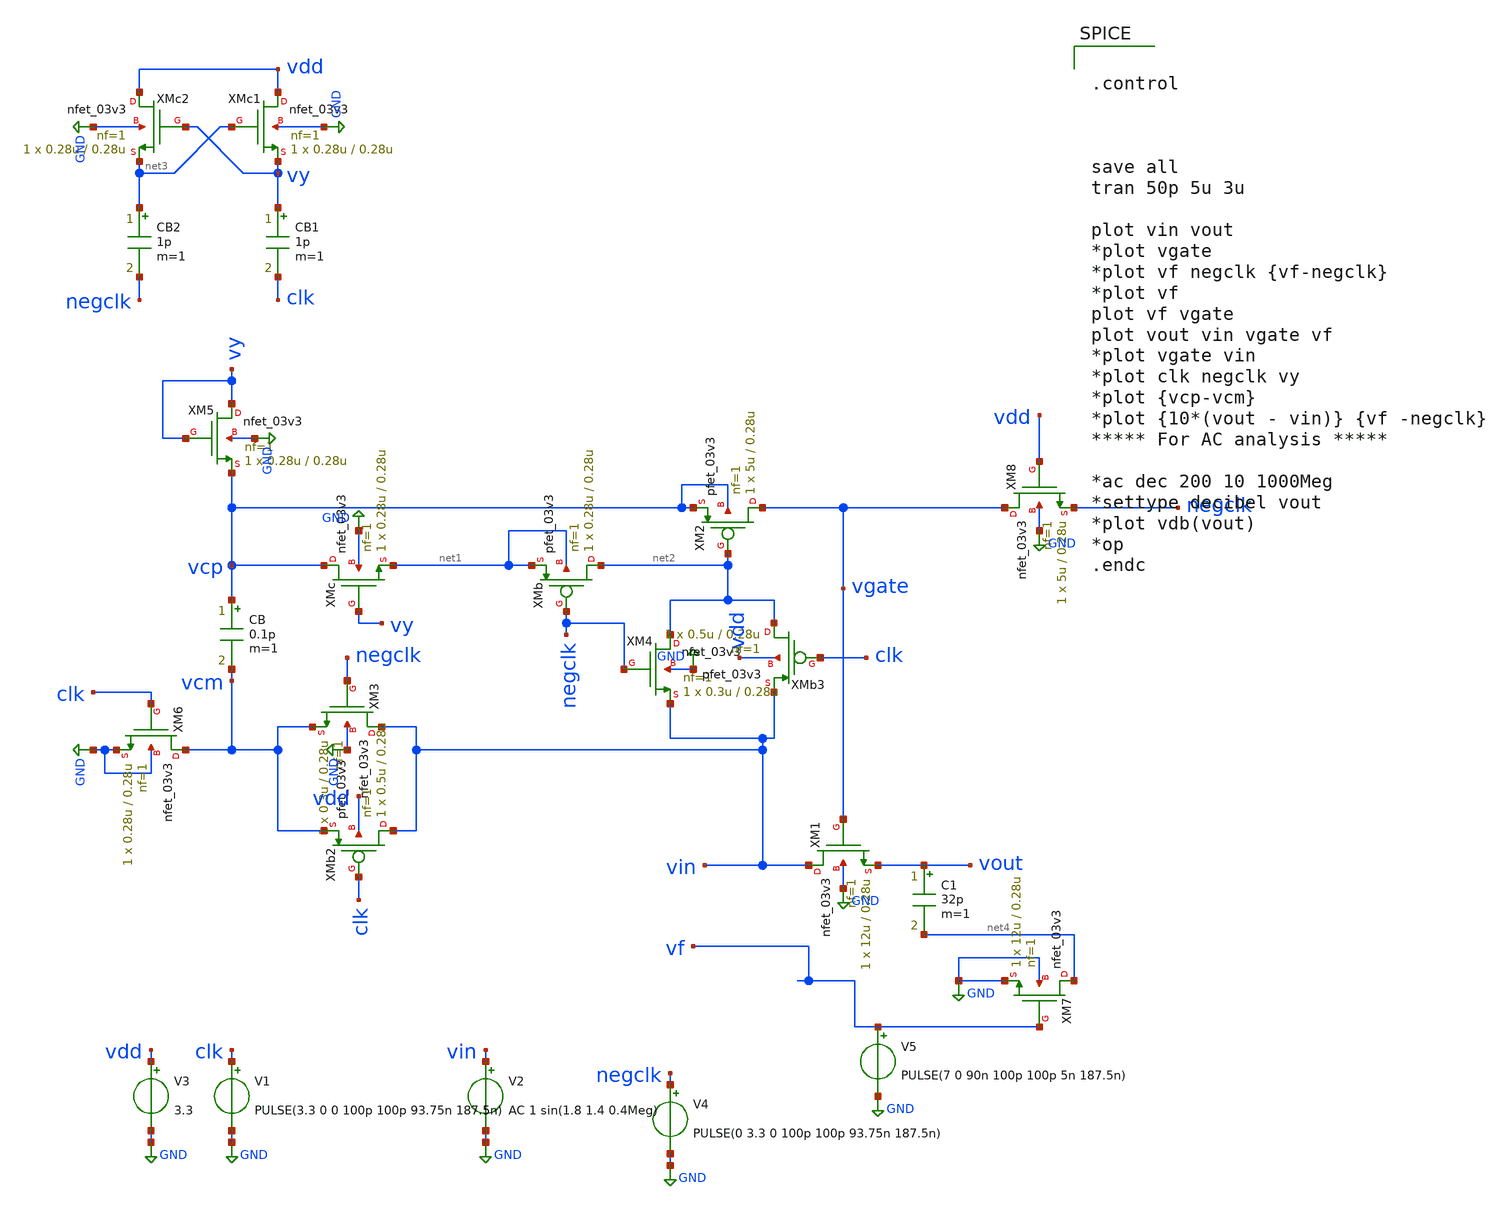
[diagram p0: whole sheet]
** sch_path: SAR_ADC/xschem/designs/sw_design/fast_bootstrap_design_bps.sch
**.subckt fast_bootstrap_design_bps
XM1 vin vgate vout GND nfet_03v3 L=0.28u W=12u nf=1 ad='int((nf+1)/2) * W/nf * 0.18u' as='int((nf+2)/2) * W/nf * 0.18u'
+ pd='2*int((nf+1)/2) * (W/nf + 0.18u)' ps='2*int((nf+2)/2) * (W/nf + 0.18u)' nrd='0.18u / W' nrs='0.18u / W'
+ sa=0 sb=0 sd=0 m=1
XM2 vgate net2 vcp vcp pfet_03v3 L=0.28u W=5u nf=1 ad='int((nf+1)/2) * W/nf * 0.18u' as='int((nf+2)/2) * W/nf * 0.18u'
+ pd='2*int((nf+1)/2) * (W/nf + 0.18u)' ps='2*int((nf+2)/2) * (W/nf + 0.18u)' nrd='0.18u / W' nrs='0.18u / W'
+ sa=0 sb=0 sd=0 m=1
XM3 vin negclk vcm GND nfet_03v3 L=0.28u W=0.3u nf=1 ad='int((nf+1)/2) * W/nf * 0.18u' as='int((nf+2)/2) * W/nf * 0.18u'
+ pd='2*int((nf+1)/2) * (W/nf + 0.18u)' ps='2*int((nf+2)/2) * (W/nf + 0.18u)' nrd='0.18u / W' nrs='0.18u / W'
+ sa=0 sb=0 sd=0 m=1
XM8 vgate vdd negclk GND nfet_03v3 L=0.28u W=5u nf=1 ad='int((nf+1)/2) * W/nf * 0.18u' as='int((nf+2)/2) * W/nf * 0.18u'
+ pd='2*int((nf+1)/2) * (W/nf + 0.18u)' ps='2*int((nf+2)/2) * (W/nf + 0.18u)' nrd='0.18u / W' nrs='0.18u / W'
+ sa=0 sb=0 sd=0 m=1
XM6 vcm clk GND GND nfet_03v3 L=0.28u W=0.28u nf=1 ad='int((nf+1)/2) * W/nf * 0.18u' as='int((nf+2)/2) * W/nf * 0.18u'
+ pd='2*int((nf+1)/2) * (W/nf + 0.18u)' ps='2*int((nf+2)/2) * (W/nf + 0.18u)' nrd='0.18u / W' nrs='0.18u / W'
+ sa=0 sb=0 sd=0 m=1
CB vcp vcm 0.1p m=1
XMb net2 negclk net1 net1 pfet_03v3 L=0.28u W=0.28u nf=1 ad='int((nf+1)/2) * W/nf * 0.18u' as='int((nf+2)/2) * W/nf * 0.18u'
+ pd='2*int((nf+1)/2) * (W/nf + 0.18u)' ps='2*int((nf+2)/2) * (W/nf + 0.18u)' nrd='0.18u / W' nrs='0.18u / W'
+ sa=0 sb=0 sd=0 m=1
XMc vcp vy net1 GND nfet_03v3 L=0.28u W=0.28u nf=1 ad='int((nf+1)/2) * W/nf * 0.18u' as='int((nf+2)/2) * W/nf * 0.18u'
+ pd='2*int((nf+1)/2) * (W/nf + 0.18u)' ps='2*int((nf+2)/2) * (W/nf + 0.18u)' nrd='0.18u / W' nrs='0.18u / W'
+ sa=0 sb=0 sd=0 m=1
XMb2 vin clk vcm vdd pfet_03v3 L=0.28u W=0.5u nf=1 ad='int((nf+1)/2) * W/nf * 0.18u' as='int((nf+2)/2) * W/nf * 0.18u'
+ pd='2*int((nf+1)/2) * (W/nf + 0.18u)' ps='2*int((nf+2)/2) * (W/nf + 0.18u)' nrd='0.18u / W' nrs='0.18u / W'
+ sa=0 sb=0 sd=0 m=1
XM4 net2 negclk vin GND nfet_03v3 L=0.28u W=0.3u nf=1 ad='int((nf+1)/2) * W/nf * 0.18u' as='int((nf+2)/2) * W/nf * 0.18u'
+ pd='2*int((nf+1)/2) * (W/nf + 0.18u)' ps='2*int((nf+2)/2) * (W/nf + 0.18u)' nrd='0.18u / W' nrs='0.18u / W'
+ sa=0 sb=0 sd=0 m=1
XMb3 net2 clk vin vdd pfet_03v3 L=0.28u W=0.5u nf=1 ad='int((nf+1)/2) * W/nf * 0.18u' as='int((nf+2)/2) * W/nf * 0.18u'
+ pd='2*int((nf+1)/2) * (W/nf + 0.18u)' ps='2*int((nf+2)/2) * (W/nf + 0.18u)' nrd='0.18u / W' nrs='0.18u / W'
+ sa=0 sb=0 sd=0 m=1
XM5 vy vy vcp GND nfet_03v3 L=0.28u W=0.28u nf=1 ad='int((nf+1)/2) * W/nf * 0.18u' as='int((nf+2)/2) * W/nf * 0.18u'
+ pd='2*int((nf+1)/2) * (W/nf + 0.18u)' ps='2*int((nf+2)/2) * (W/nf + 0.18u)' nrd='0.18u / W' nrs='0.18u / W'
+ sa=0 sb=0 sd=0 m=1
XMc1 vdd net3 vy GND nfet_03v3 L=0.28u W=0.28u nf=1 ad='int((nf+1)/2) * W/nf * 0.18u' as='int((nf+2)/2) * W/nf * 0.18u'
+ pd='2*int((nf+1)/2) * (W/nf + 0.18u)' ps='2*int((nf+2)/2) * (W/nf + 0.18u)' nrd='0.18u / W' nrs='0.18u / W'
+ sa=0 sb=0 sd=0 m=1
XMc2 vdd vy net3 GND nfet_03v3 L=0.28u W=0.28u nf=1 ad='int((nf+1)/2) * W/nf * 0.18u' as='int((nf+2)/2) * W/nf * 0.18u'
+ pd='2*int((nf+1)/2) * (W/nf + 0.18u)' ps='2*int((nf+2)/2) * (W/nf + 0.18u)' nrd='0.18u / W' nrs='0.18u / W'
+ sa=0 sb=0 sd=0 m=1
CB1 vy clk 1p m=1
CB2 net3 negclk 1p m=1
V1 clk GND PULSE(3.3 0 0 100p 100p 93.75n 187.5n)
V2 vin GND AC 1 sin(1.8 1.4 0.4Meg)
V3 vdd GND 3.3
V4 negclk GND PULSE(0 3.3 0 100p 100p 93.75n 187.5n)
C1 vout net4 32p m=1
V5 vf GND PULSE(7 0 90n 100p 100p 5n 187.5n)
XM7 net4 vf GND GND nfet_03v3 L=0.28u W=12u nf=1 ad='int((nf+1)/2) * W/nf * 0.18u' as='int((nf+2)/2) * W/nf * 0.18u'
+ pd='2*int((nf+1)/2) * (W/nf + 0.18u)' ps='2*int((nf+2)/2) * (W/nf + 0.18u)' nrd='0.18u / W' nrs='0.18u / W'
+ sa=0 sb=0 sd=0 m=1
**** begin user architecture code


.control



save all
tran 50p 5u 3u

plot vin vout
*plot vgate
*plot vf negclk {vf-negclk}
*plot vf
plot vf vgate
plot vout vin vgate vf
*plot vgate vin
*plot clk negclk vy
*plot {vcp-vcm}
*plot {10*(vout - vin)} {vf -negclk}
***** For AC analysis *****

*ac dec 200 10 1000Meg
*settype decibel vout
*plot vdb(vout)
*op
.endc


.include $env(PDK_ROOT)/$env(PDK)/libs.tech/ngspice/design.ngspice
.lib $env(PDK_ROOT)/$env(PDK)/libs.tech/ngspice/sm141064.ngspice typical

**** end user architecture code
**.ends
.GLOBAL GND
.end
